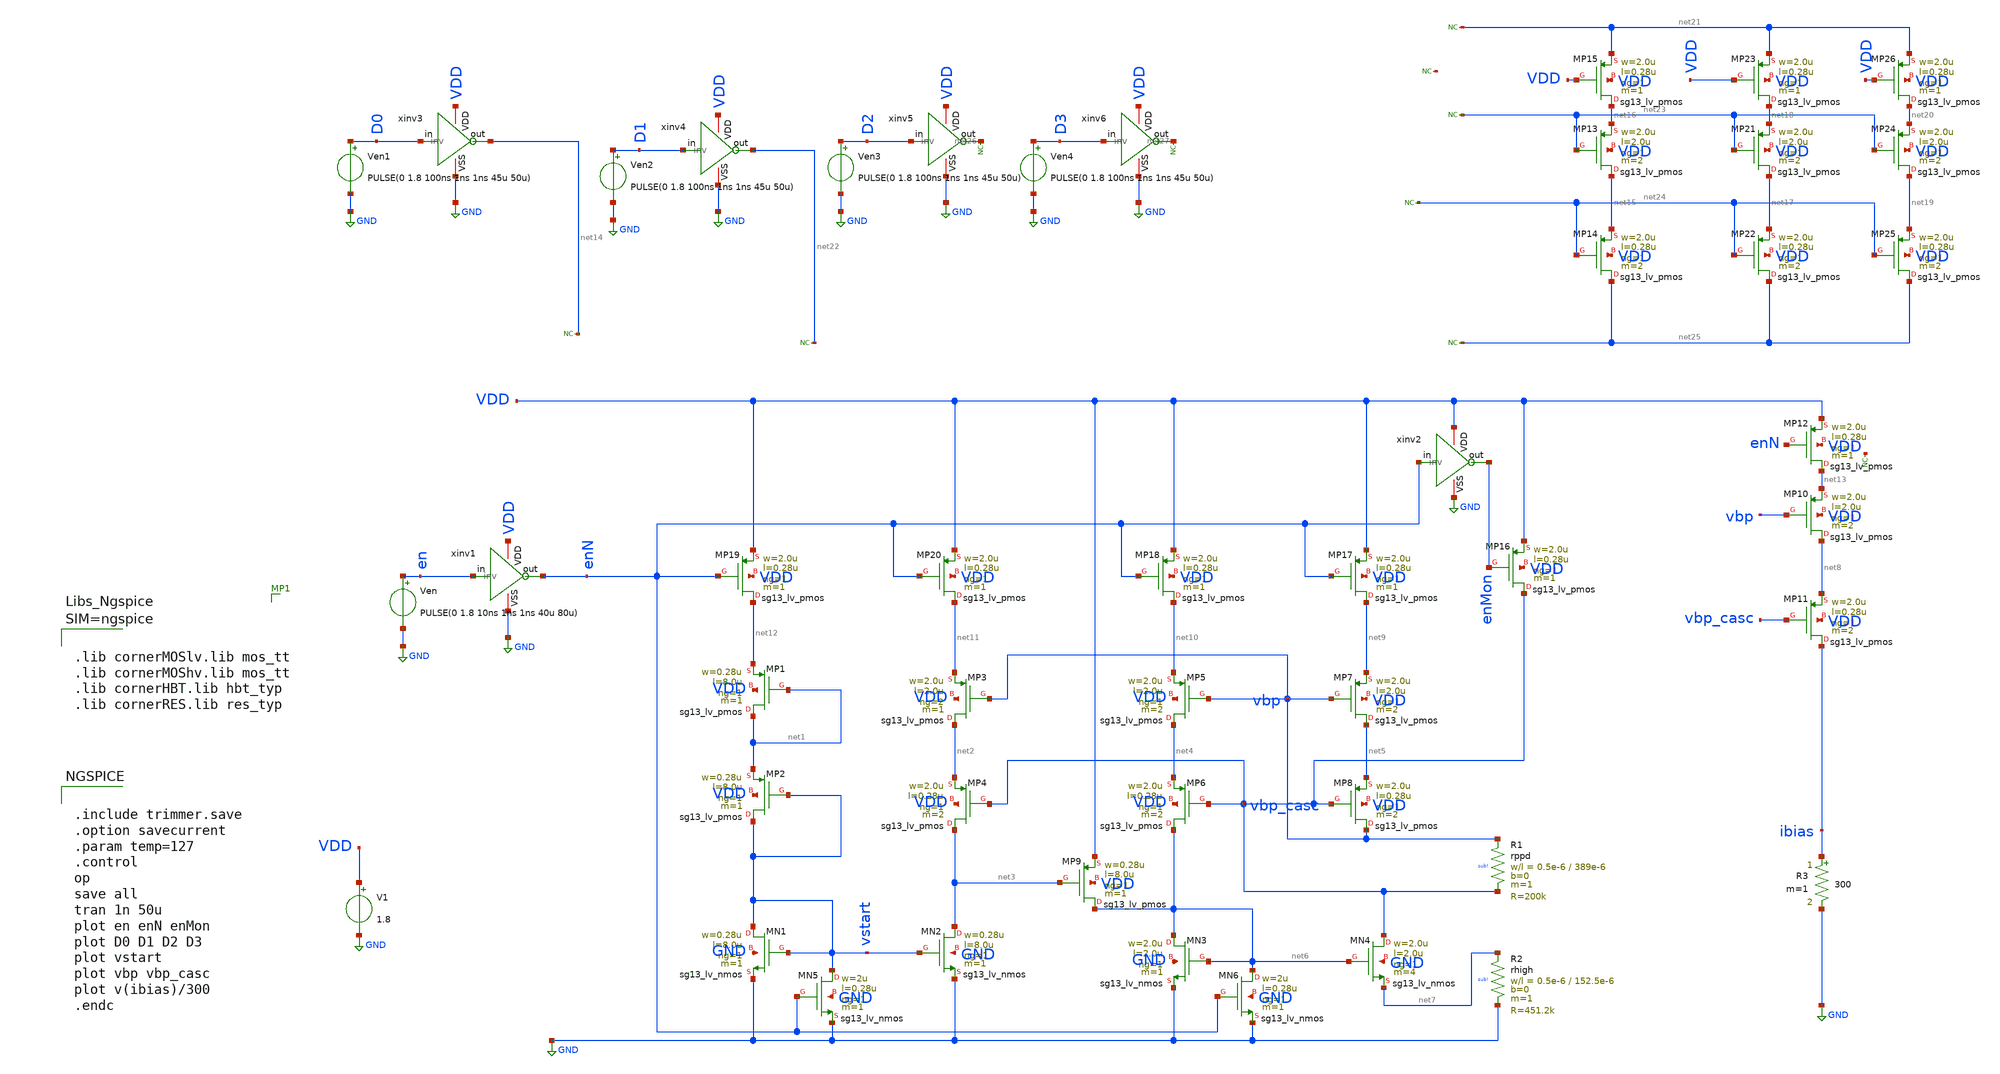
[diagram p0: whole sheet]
** sch_path: blocks/composite/dpi_adexp_neuron/design_data/xschem/trimmer_test.sch
**.subckt trimmer_test
XMP1 net1 net1 net12 VDD sg13_lv_pmos w=0.28u l=8.0u ng=1 m=1 mm_ok=1
XMP2 vstart vstart net1 VDD sg13_lv_pmos w=0.28u l=8.0u ng=1 m=1 mm_ok=1
XMN2 net3 vstart GND GND sg13_lv_nmos w=0.28u l=8.0u ng=1 m=1 mm_ok=1
XMN1 vstart vstart GND GND sg13_lv_nmos w=0.28u l=8.0u ng=1 m=1 mm_ok=1
XMP3 net2 vbp net11 VDD sg13_lv_pmos w=2.0u l=2.0u ng=2 m=1 mm_ok=1
XMP4 net3 vbp_casc net2 VDD sg13_lv_pmos w=2.0u l=0.28u ng=1 m=2 mm_ok=1
XMP5 net4 vbp net10 VDD sg13_lv_pmos w=2.0u l=2.0u ng=1 m=2 mm_ok=1
XMP6 net6 vbp_casc net4 VDD sg13_lv_pmos w=2.0u l=0.28u ng=1 m=2 mm_ok=1
XMP7 net5 vbp net9 VDD sg13_lv_pmos w=2.0u l=2.0u ng=1 m=2 mm_ok=1
XMP8 vbp vbp_casc net5 VDD sg13_lv_pmos w=2.0u l=0.28u ng=1 m=2 mm_ok=1
XMP9 net6 net3 VDD VDD sg13_lv_pmos w=0.28u l=8.0u ng=1 m=1 mm_ok=1
XMN3 net6 net6 GND GND sg13_lv_nmos w=2.0u l=2.0u ng=1 m=1 mm_ok=1
XMN4 vbp_casc net6 net7 GND sg13_lv_nmos w=2.0u l=2.0u ng=1 m=4 mm_ok=1
XR1 vbp vbp_casc sub! rppd w=0.5e-6 l=389e-6 m=1 b=0 mm_ok=1
XR2 net7 GND sub! rhigh w=0.5e-6 l=152.5e-6 m=1 b=0 mm_ok=1
R3 ibias GND 300 m=1
XMP10 net8 vbp net13 VDD sg13_lv_pmos w=2.0u l=2.0u ng=1 m=2 mm_ok=1
XMP11 ibias vbp_casc net8 VDD sg13_lv_pmos w=2.0u l=0.28u ng=1 m=2 mm_ok=1
XMP16 vbp_casc enMon VDD VDD sg13_lv_pmos w=2.0u l=0.28u ng=1 m=1 mm_ok=1
XMP17 net9 enN VDD VDD sg13_lv_pmos w=2.0u l=0.28u ng=1 m=1 mm_ok=1
XMP18 net10 enN VDD VDD sg13_lv_pmos w=2.0u l=0.28u ng=1 m=1 mm_ok=1
XMP19 net12 enN VDD VDD sg13_lv_pmos w=2.0u l=0.28u ng=1 m=1 mm_ok=1
XMP20 net11 enN VDD VDD sg13_lv_pmos w=2.0u l=0.28u ng=1 m=1 mm_ok=1
XMN5 vstart enN GND GND sg13_lv_nmos w=2u l=0.28u ng=1 m=1 mm_ok=1
XMN6 net6 enN GND GND sg13_lv_nmos w=2u l=0.28u ng=1 m=1 mm_ok=1
V1 VDD GND 1.8
Ven en GND PULSE(0 1.8 10ns 1ns 1ns 40u 80u)
xinv1 VDD en enN GND inv
xinv2 VDD enN enMon GND inv
XMP12 net13 enN VDD VDD sg13_lv_pmos w=2.0u l=0.28u ng=1 m=1 mm_ok=1
Ven1 D0 GND PULSE(0 1.8 100ns 1ns 1ns 45u 50u)

xinv3 VDD D0 net14 GND inv
XMP13 net15 net23 net16 VDD sg13_lv_pmos w=2.0u l=2.0u ng=1 m=2 mm_ok=1
XMP14 net25 net24 net15 VDD sg13_lv_pmos w=2.0u l=0.28u ng=1 m=2 mm_ok=1
XMP15 net16 VDD net21 VDD sg13_lv_pmos w=2.0u l=0.28u ng=1 m=1 mm_ok=1
XMP21 net17 net23 net18 VDD sg13_lv_pmos w=2.0u l=2.0u ng=1 m=2 mm_ok=1
XMP22 net25 net24 net17 VDD sg13_lv_pmos w=2.0u l=0.28u ng=1 m=2 mm_ok=1
XMP23 net18 VDD net21 VDD sg13_lv_pmos w=2.0u l=0.28u ng=1 m=1 mm_ok=1
XMP24 net19 net23 net20 VDD sg13_lv_pmos w=2.0u l=2.0u ng=1 m=2 mm_ok=1
XMP25 net25 net24 net19 VDD sg13_lv_pmos w=2.0u l=0.28u ng=1 m=2 mm_ok=1
XMP26 net20 VDD net21 VDD sg13_lv_pmos w=2.0u l=0.28u ng=1 m=1 mm_ok=1
Ven2 D1 GND PULSE(0 1.8 100ns 1ns 1ns 45u 50u)

xinv4 VDD D1 net22 GND inv
Ven3 D2 GND PULSE(0 1.8 100ns 1ns 1ns 45u 50u)

xinv5 VDD D2 net26 GND inv
Ven4 D3 GND PULSE(0 1.8 100ns 1ns 1ns 45u 50u)

xinv6 VDD D3 net27 GND inv
* noconn #net28
* noconn #net26
* noconn #net27
* noconn #net29
* noconn #net21
* noconn #net23
* noconn #net24
* noconn #net25
* noconn #net22
* noconn #net14
**** begin user architecture code


.include trimmer.save
.option savecurrent
.param temp=127
.control
op
save all
tran 1n 50u
plot en enN enMon
plot D0 D1 D2 D3
plot vstart
plot vbp vbp_casc
plot v(ibias)/300
.endc





.lib cornerMOSlv.lib mos_tt
.lib cornerMOShv.lib mos_tt
.lib cornerHBT.lib hbt_typ
.lib cornerRES.lib res_typ



**** end user architecture code
**.ends

* expanding   symbol:  inv.sym # of pins=4
** sym_path: blocks/composite/dpi_adexp_neuron/design_data/xschem/dev/inv.sym
** sch_path: blocks/composite/dpi_adexp_neuron/design_data/xschem/dev/inv.sch
.subckt inv VDD in out VSS
*.iopin VDD
*.ipin in
*.iopin VSS
*.opin out
XM1 out in VSS VSS sg13_lv_nmos w=2.0u l=0.28u ng=1 m=1 mm_ok=1
XM2 out in VDD VDD sg13_lv_pmos w=2.0u l=0.28u ng=1 m=1 mm_ok=1
.ends

.GLOBAL GND
.end
